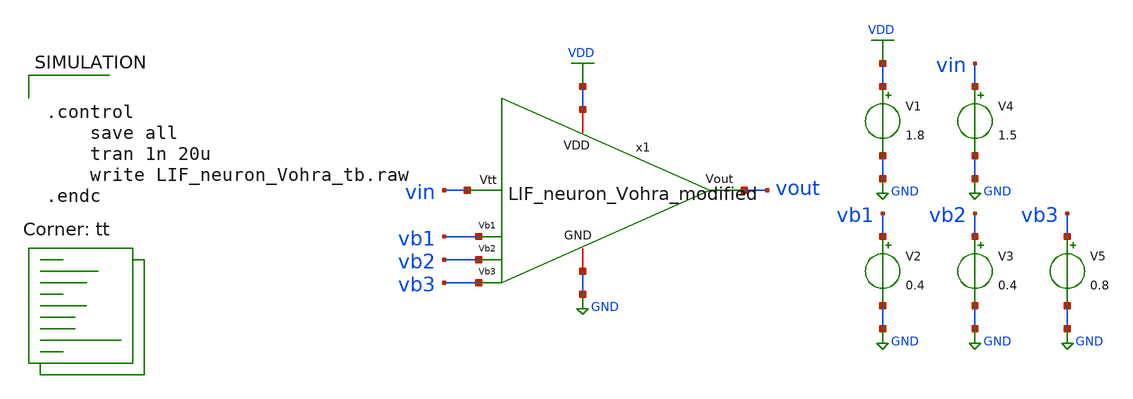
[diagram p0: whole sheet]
** sch_path: LIF_neuron/LIF_neuron_Vohra_modified_tb.sch
**.subckt LIF_neuron_Vohra_modified_tb
V1 VDD GND 1.8
V2 vb1 GND 0.4
V3 vb2 GND 0.4
V4 vin GND 1.5
x1 VDD vout vb1 GND vb2 vb3 vin LIF_neuron_Vohra_modified
V5 vb3 GND 0.8
**** begin user architecture code


.control
	save all
	tran 1n 20u
	write LIF_neuron_Vohra_tb.raw
.endc


.lib $::SKYWATER_MODELS/sky130.lib.spice tt
**** end user architecture code
**.ends

* expanding   symbol:
*+  /home/ricardoatt/RATT_repos/Proyectos_xschem/LIF_neuron/LIF_neuron_Vohra_modified.sym # of pins=7
** sym_path: LIF_neuron/LIF_neuron_Vohra_modified.sym
** sch_path: LIF_neuron/LIF_neuron_Vohra_modified.sch
.subckt LIF_neuron_Vohra_modified VDD Vout Vb1 GND Vb2 Vb3 Vtt
*.ipin Vtt
*.iopin GND
*.ipin Vb1
*.ipin Vb2
*.iopin VDD
*.opin Vout
*.ipin Vb3
XM1 net3 Vtt GND GND sky130_fd_pr__nfet_01v8 L=1 W=0.6 nf=1 ad='int((nf+1)/2) * W/nf * 0.29' as='int((nf+2)/2) * W/nf * 0.29'
+ pd='2*int((nf+1)/2) * (W/nf + 0.29)' ps='2*int((nf+2)/2) * (W/nf + 0.29)' nrd='0.29 / W' nrs='0.29 / W'
+ sa=0 sb=0 sd=0 mult=1 m=1
XM3 net3 net3 VDD VDD sky130_fd_pr__pfet_01v8 L=1 W=0.6 nf=1 ad='int((nf+1)/2) * W/nf * 0.29' as='int((nf+2)/2) * W/nf * 0.29'
+ pd='2*int((nf+1)/2) * (W/nf + 0.29)' ps='2*int((nf+2)/2) * (W/nf + 0.29)' nrd='0.29 / W' nrs='0.29 / W'
+ sa=0 sb=0 sd=0 mult=1 m=1
XM13 net2 Vb1 GND GND sky130_fd_pr__nfet_01v8 L=0.5 W=5 nf=1 ad='int((nf+1)/2) * W/nf * 0.29' as='int((nf+2)/2) * W/nf * 0.29'
+ pd='2*int((nf+1)/2) * (W/nf + 0.29)' ps='2*int((nf+2)/2) * (W/nf + 0.29)' nrd='0.29 / W' nrs='0.29 / W'
+ sa=0 sb=0 sd=0 mult=1 m=1
XM12 rc net1 net2 GND sky130_fd_pr__nfet_01v8 L=1 W=1 nf=1 ad='int((nf+1)/2) * W/nf * 0.29' as='int((nf+2)/2) * W/nf * 0.29'
+ pd='2*int((nf+1)/2) * (W/nf + 0.29)' ps='2*int((nf+2)/2) * (W/nf + 0.29)' nrd='0.29 / W' nrs='0.29 / W'
+ sa=0 sb=0 sd=0 mult=1 m=1
XM11 rc net1 VDD VDD sky130_fd_pr__pfet_01v8 L=1 W=1 nf=1 ad='int((nf+1)/2) * W/nf * 0.29' as='int((nf+2)/2) * W/nf * 0.29'
+ pd='2*int((nf+1)/2) * (W/nf + 0.29)' ps='2*int((nf+2)/2) * (W/nf + 0.29)' nrd='0.29 / W' nrs='0.29 / W'
+ sa=0 sb=0 sd=0 mult=1 m=1
XC1 rc GND sky130_fd_pr__cap_mim_m3_1 W=21 L=1 MF=1 m=1
XM14 u rc GND GND sky130_fd_pr__nfet_01v8 L=4 W=1 nf=1 ad='int((nf+1)/2) * W/nf * 0.29' as='int((nf+2)/2) * W/nf * 0.29'
+ pd='2*int((nf+1)/2) * (W/nf + 0.29)' ps='2*int((nf+2)/2) * (W/nf + 0.29)' nrd='0.29 / W' nrs='0.29 / W'
+ sa=0 sb=0 sd=0 mult=1 m=1
XM4 u net3 VDD VDD sky130_fd_pr__pfet_01v8 L=1 W=1 nf=1 ad='int((nf+1)/2) * W/nf * 0.29' as='int((nf+2)/2) * W/nf * 0.29'
+ pd='2*int((nf+1)/2) * (W/nf + 0.29)' ps='2*int((nf+2)/2) * (W/nf + 0.29)' nrd='0.29 / W' nrs='0.29 / W'
+ sa=0 sb=0 sd=0 mult=1 m=1
XC2 u GND sky130_fd_pr__cap_mim_m3_1 W=10 L=1 MF=50 m=50
XM5 u Vb2 GND GND sky130_fd_pr__nfet_01v8 L=1 W=2 nf=1 ad='int((nf+1)/2) * W/nf * 0.29' as='int((nf+2)/2) * W/nf * 0.29'
+ pd='2*int((nf+1)/2) * (W/nf + 0.29)' ps='2*int((nf+2)/2) * (W/nf + 0.29)' nrd='0.29 / W' nrs='0.29 / W'
+ sa=0 sb=0 sd=0 mult=1 m=1
XM6 net4 Vb3 GND GND sky130_fd_pr__nfet_01v8 L=0.5 W=1 nf=1 ad='int((nf+1)/2) * W/nf * 0.29' as='int((nf+2)/2) * W/nf * 0.29'
+ pd='2*int((nf+1)/2) * (W/nf + 0.29)' ps='2*int((nf+2)/2) * (W/nf + 0.29)' nrd='0.29 / W' nrs='0.29 / W'
+ sa=0 sb=0 sd=0 mult=1 m=1
XM7 net1 u net4 GND sky130_fd_pr__nfet_01v8 L=1 W=1 nf=1 ad='int((nf+1)/2) * W/nf * 0.29' as='int((nf+2)/2) * W/nf * 0.29'
+ pd='2*int((nf+1)/2) * (W/nf + 0.29)' ps='2*int((nf+2)/2) * (W/nf + 0.29)' nrd='0.29 / W' nrs='0.29 / W'
+ sa=0 sb=0 sd=0 mult=1 m=1
XM8 net1 u VDD VDD sky130_fd_pr__pfet_01v8 L=1 W=1 nf=1 ad='int((nf+1)/2) * W/nf * 0.29' as='int((nf+2)/2) * W/nf * 0.29'
+ pd='2*int((nf+1)/2) * (W/nf + 0.29)' ps='2*int((nf+2)/2) * (W/nf + 0.29)' nrd='0.29 / W' nrs='0.29 / W'
+ sa=0 sb=0 sd=0 mult=1 m=1
XM9 Vout net1 net4 GND sky130_fd_pr__nfet_01v8 L=1 W=1 nf=1 ad='int((nf+1)/2) * W/nf * 0.29' as='int((nf+2)/2) * W/nf * 0.29'
+ pd='2*int((nf+1)/2) * (W/nf + 0.29)' ps='2*int((nf+2)/2) * (W/nf + 0.29)' nrd='0.29 / W' nrs='0.29 / W'
+ sa=0 sb=0 sd=0 mult=1 m=1
XM10 Vout net1 VDD VDD sky130_fd_pr__pfet_01v8 L=1 W=5 nf=1 ad='int((nf+1)/2) * W/nf * 0.29' as='int((nf+2)/2) * W/nf * 0.29'
+ pd='2*int((nf+1)/2) * (W/nf + 0.29)' ps='2*int((nf+2)/2) * (W/nf + 0.29)' nrd='0.29 / W' nrs='0.29 / W'
+ sa=0 sb=0 sd=0 mult=1 m=1
.ends

.GLOBAL GND
.GLOBAL VDD
.end
